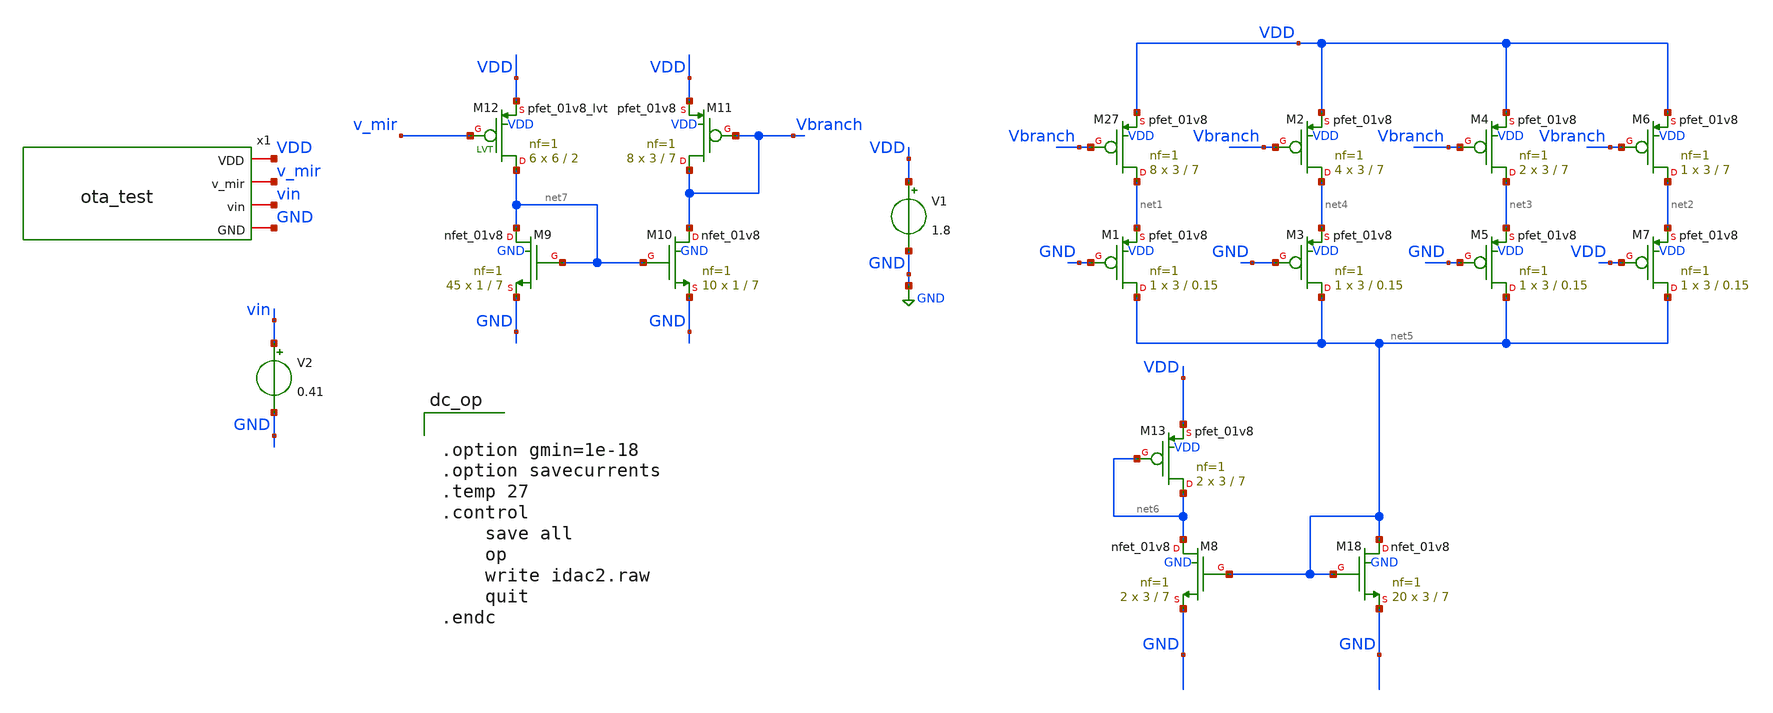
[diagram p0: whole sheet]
** sch_path: xschem/archive/old_blocks/idac2.sch
**.subckt idac2
XM27 net1 Vbranch VDD VDD sky130_fd_pr__pfet_01v8 L=7 W=3 nf=1 ad='int((1 + 1)/2) * 3 / 1 * 0.29' as='int((1 + 2)/2) * 3 / 1 * 0.29'
+ pd='2*int((1 + 1)/2) * (3 / 1 + 0.29)' ps='2*int((1 + 2)/2) * (3 / 1 + 0.29)' nrd='0.29 / 3 ' nrs='0.29 / 3 '
+ sa=0 sb=0 sd=0 mult=8 m=8
XM1 net5 GND net1 VDD sky130_fd_pr__pfet_01v8 L=0.15 W=3 nf=1 ad='int((1 + 1)/2) * 3 / 1 * 0.29' as='int((1 + 2)/2) * 3 / 1 * 0.29'
+ pd='2*int((1 + 1)/2) * (3 / 1 + 0.29)' ps='2*int((1 + 2)/2) * (3 / 1 + 0.29)' nrd='0.29 / 3 ' nrs='0.29 / 3 '
+ sa=0 sb=0 sd=0 mult=1 m=1
XM2 net4 Vbranch VDD VDD sky130_fd_pr__pfet_01v8 L=7 W=3 nf=1 ad='int((1 + 1)/2) * 3 / 1 * 0.29' as='int((1 + 2)/2) * 3 / 1 * 0.29'
+ pd='2*int((1 + 1)/2) * (3 / 1 + 0.29)' ps='2*int((1 + 2)/2) * (3 / 1 + 0.29)' nrd='0.29 / 3 ' nrs='0.29 / 3 '
+ sa=0 sb=0 sd=0 mult=4 m=4
XM3 net5 GND net4 VDD sky130_fd_pr__pfet_01v8 L=0.15 W=3 nf=1 ad='int((1 + 1)/2) * 3 / 1 * 0.29' as='int((1 + 2)/2) * 3 / 1 * 0.29'
+ pd='2*int((1 + 1)/2) * (3 / 1 + 0.29)' ps='2*int((1 + 2)/2) * (3 / 1 + 0.29)' nrd='0.29 / 3 ' nrs='0.29 / 3 '
+ sa=0 sb=0 sd=0 mult=1 m=1
XM4 net3 Vbranch VDD VDD sky130_fd_pr__pfet_01v8 L=7 W=3 nf=1 ad='int((1 + 1)/2) * 3 / 1 * 0.29' as='int((1 + 2)/2) * 3 / 1 * 0.29'
+ pd='2*int((1 + 1)/2) * (3 / 1 + 0.29)' ps='2*int((1 + 2)/2) * (3 / 1 + 0.29)' nrd='0.29 / 3 ' nrs='0.29 / 3 '
+ sa=0 sb=0 sd=0 mult=2 m=2
XM5 net5 GND net3 VDD sky130_fd_pr__pfet_01v8 L=0.15 W=3 nf=1 ad='int((1 + 1)/2) * 3 / 1 * 0.29' as='int((1 + 2)/2) * 3 / 1 * 0.29'
+ pd='2*int((1 + 1)/2) * (3 / 1 + 0.29)' ps='2*int((1 + 2)/2) * (3 / 1 + 0.29)' nrd='0.29 / 3 ' nrs='0.29 / 3 '
+ sa=0 sb=0 sd=0 mult=1 m=1
XM6 net2 Vbranch VDD VDD sky130_fd_pr__pfet_01v8 L=7 W=3 nf=1 ad='int((1 + 1)/2) * 3 / 1 * 0.29' as='int((1 + 2)/2) * 3 / 1 * 0.29'
+ pd='2*int((1 + 1)/2) * (3 / 1 + 0.29)' ps='2*int((1 + 2)/2) * (3 / 1 + 0.29)' nrd='0.29 / 3 ' nrs='0.29 / 3 '
+ sa=0 sb=0 sd=0 mult=1 m=1
XM7 net5 VDD net2 VDD sky130_fd_pr__pfet_01v8 L=0.15 W=3 nf=1 ad='int((1 + 1)/2) * 3 / 1 * 0.29' as='int((1 + 2)/2) * 3 / 1 * 0.29'
+ pd='2*int((1 + 1)/2) * (3 / 1 + 0.29)' ps='2*int((1 + 2)/2) * (3 / 1 + 0.29)' nrd='0.29 / 3 ' nrs='0.29 / 3 '
+ sa=0 sb=0 sd=0 mult=1 m=1
XM18 net5 net5 GND GND sky130_fd_pr__nfet_01v8 L=7 W=3 nf=1 ad='int((nf+1)/2) * W/nf * 0.29' as='int((nf+2)/2) * W/nf * 0.29'
+ pd='2*int((nf+1)/2) * (W/nf + 0.29)' ps='2*int((nf+2)/2) * (W/nf + 0.29)' nrd='0.29 / W' nrs='0.29 / W'
+ sa=0 sb=0 sd=0 mult=20 m=20
XM8 net6 net5 GND GND sky130_fd_pr__nfet_01v8 L=7 W=3 nf=1 ad='int((nf+1)/2) * W/nf * 0.29' as='int((nf+2)/2) * W/nf * 0.29'
+ pd='2*int((nf+1)/2) * (W/nf + 0.29)' ps='2*int((nf+2)/2) * (W/nf + 0.29)' nrd='0.29 / W' nrs='0.29 / W'
+ sa=0 sb=0 sd=0 mult=2 m=2
XM9 net7 net7 GND GND sky130_fd_pr__nfet_01v8 L=7 W=1 nf=1 ad='int((nf+1)/2) * W/nf * 0.29' as='int((nf+2)/2) * W/nf * 0.29'
+ pd='2*int((nf+1)/2) * (W/nf + 0.29)' ps='2*int((nf+2)/2) * (W/nf + 0.29)' nrd='0.29 / W' nrs='0.29 / W'
+ sa=0 sb=0 sd=0 mult=45 m=45
XM10 Vbranch net7 GND GND sky130_fd_pr__nfet_01v8 L=7 W=1 nf=1 ad='int((nf+1)/2) * W/nf * 0.29' as='int((nf+2)/2) * W/nf * 0.29'
+ pd='2*int((nf+1)/2) * (W/nf + 0.29)' ps='2*int((nf+2)/2) * (W/nf + 0.29)' nrd='0.29 / W' nrs='0.29 / W'
+ sa=0 sb=0 sd=0 mult=10 m=10
XM11 Vbranch Vbranch VDD VDD sky130_fd_pr__pfet_01v8 L=7 W=3 nf=1 ad='int((1 + 1)/2) * 3 / 1 * 0.29'
+ as='int((1 + 2)/2) * 3 / 1 * 0.29' pd='2*int((1 + 1)/2) * (3 / 1 + 0.29)' ps='2*int((1 + 2)/2) * (3 / 1 + 0.29)'
+ nrd='0.29 / 3 ' nrs='0.29 / 3 ' sa=0 sb=0 sd=0 mult=8 m=8
V1 VDD GND 1.8
x1 VDD v_mir vin GND ota_test
XM12 net7 v_mir VDD VDD sky130_fd_pr__pfet_01v8_lvt L=2 W=6 nf=1 ad='int((1 + 1)/2) * 6 / 1 * 0.29' as='int((1 + 2)/2) * 6 / 1 * 0.29'
+ pd='2*int((1 + 1)/2) * (6 / 1 + 0.29)' ps='2*int((1 + 2)/2) * (6 / 1 + 0.29)' nrd='0.29 / 6 ' nrs='0.29 / 6 '
+ sa=0 sb=0 sd=0 mult=6 m=6
V2 vin GND 0.41
XM13 net6 net6 VDD VDD sky130_fd_pr__pfet_01v8 L=7 W=3 nf=1 ad='int((1 + 1)/2) * 3 / 1 * 0.29' as='int((1 + 2)/2) * 3 / 1 * 0.29'
+ pd='2*int((1 + 1)/2) * (3 / 1 + 0.29)' ps='2*int((1 + 2)/2) * (3 / 1 + 0.29)' nrd='0.29 / 3 ' nrs='0.29 / 3 '
+ sa=0 sb=0 sd=0 mult=2 m=2
**** begin user architecture code


.option gmin=1e-18
.option savecurrents
.temp 27
.control
    save all
    op
    write idac2.raw
    quit
.endc




** opencircuitdesign pdks install
.lib $::SKYWATER_MODELS/sky130.lib.spice ss

**** end user architecture code
**.ends

* expanding   symbol:  ota_test.sym # of pins=4
** sym_path: xschem/archive/old_blocks/ota_test.sym
** sch_path: xschem/archive/old_blocks/ota_test.sch
.subckt ota_test VDD v_mir vin GND
*.iopin v_mir
*.iopin vin
*.iopin GND
*.iopin VDD
XR1 GND net2 GND sky130_fd_pr__res_xhigh_po_1p41 L=20 mult=1 m=1
Vmeas VDD net3 0
.save i(vmeas)
XM2 v_mir net1 net2 GND sky130_fd_pr__nfet_01v8_lvt L=1 W=3 nf=1 ad='int((1 + 1)/2) * 3 / 1 * 0.29' as='int((1 + 2)/2) * 3 / 1 * 0.29'
+ pd='2*int((1 + 1)/2) * (3 / 1 + 0.29)' ps='2*int((1 + 2)/2) * (3 / 1 + 0.29)' nrd='0.29 / 3 ' nrs='0.29 / 3 '
+ sa=0 sb=0 sd=0 mult=6 m=6
XM1 v_mir v_mir net3 VDD sky130_fd_pr__pfet_01v8_lvt L=2 W=6 nf=1 ad='int((1 + 1)/2) * 6 / 1 * 0.29'
+ as='int((1 + 2)/2) * 6 / 1 * 0.29' pd='2*int((1 + 1)/2) * (6 / 1 + 0.29)' ps='2*int((1 + 2)/2) * (6 / 1 + 0.29)'
+ nrd='0.29 / 6 ' nrs='0.29 / 6 ' sa=0 sb=0 sd=0 mult=6 m=6
x1 VDD VDD net1 vin net2 net4 GND OTA_Gm_Cell_v2
.ends


* expanding   symbol:  archive/ota_gm_cell/OTA_Gm_Cell_v2.sym # of pins=7
** sym_path: xschem/archive/ota_gm_cell/OTA_Gm_Cell_v2.sym
** sch_path: xschem/archive/ota_gm_cell/OTA_Gm_Cell_v2.sch
.subckt OTA_Gm_Cell_v2 AVDDH EN VOUT VINP VINN MN_TAIL_BIAS GNDA
*.iopin AVDDH
*.iopin GNDA
*.iopin VOUT
*.iopin MN_TAIL_BIAS
*.ipin EN
*.iopin VINP
*.iopin VINN
XM1 VBP_TOP MN_TAIL_BIAS net4 GND sky130_fd_pr__nfet_01v8 L=4 W=10 nf=1 ad='int((1 + 1)/2) * 10 / 1 * 0.29'
+ as='int((1 + 2)/2) * 10 / 1 * 0.29' pd='2*int((1 + 1)/2) * (10 / 1 + 0.29)' ps='2*int((1 + 2)/2) * (10 / 1 + 0.29)'
+ nrd='0.29 / 10 ' nrs='0.29 / 10 ' sa=0 sb=0 sd=0 mult=16 m=16
XM3 net1 VBP_TOP AVDDH VDD sky130_fd_pr__pfet_01v8 L=2 W=2 nf=1 ad='int((1 + 1)/2) * 2 / 1 * 0.29' as='int((1 + 2)/2) * 2 / 1 * 0.29'
+ pd='2*int((1 + 1)/2) * (2 / 1 + 0.29)' ps='2*int((1 + 2)/2) * (2 / 1 + 0.29)' nrd='0.29 / 2 ' nrs='0.29 / 2 '
+ sa=0 sb=0 sd=0 mult=4 m=4
XM4 net2 VBP_TOP AVDDH VDD sky130_fd_pr__pfet_01v8 L=2 W=2 nf=1 ad='int((1 + 1)/2) * 2 / 1 * 0.29' as='int((1 + 2)/2) * 2 / 1 * 0.29'
+ pd='2*int((1 + 1)/2) * (2 / 1 + 0.29)' ps='2*int((1 + 2)/2) * (2 / 1 + 0.29)' nrd='0.29 / 2 ' nrs='0.29 / 2 '
+ sa=0 sb=0 sd=0 mult=1 m=1
XM5 VBP_TOP VBP_CASC net1 VDD sky130_fd_pr__pfet_01v8 L=2 W=2 nf=1 ad='int((1 + 1)/2) * 2 / 1 * 0.29'
+ as='int((1 + 2)/2) * 2 / 1 * 0.29' pd='2*int((1 + 1)/2) * (2 / 1 + 0.29)' ps='2*int((1 + 2)/2) * (2 / 1 + 0.29)'
+ nrd='0.29 / 2 ' nrs='0.29 / 2 ' sa=0 sb=0 sd=0 mult=2 m=2
XM6 net11 VBP_CASC net2 VDD sky130_fd_pr__pfet_01v8 L=2 W=2 nf=1 ad='int((1 + 1)/2) * 2 / 1 * 0.29' as='int((1 + 2)/2) * 2 / 1 * 0.29'
+ pd='2*int((1 + 1)/2) * (2 / 1 + 0.29)' ps='2*int((1 + 2)/2) * (2 / 1 + 0.29)' nrd='0.29 / 2 ' nrs='0.29 / 2 '
+ sa=0 sb=0 sd=0 mult=2 m=2
XM7 VOUT MN_TAIL_BIAS net5 GND sky130_fd_pr__nfet_01v8 L=4 W=10 nf=1 ad='int((1 + 1)/2) * 10 / 1 * 0.29'
+ as='int((1 + 2)/2) * 10 / 1 * 0.29' pd='2*int((1 + 1)/2) * (10 / 1 + 0.29)' ps='2*int((1 + 2)/2) * (10 / 1 + 0.29)'
+ nrd='0.29 / 10 ' nrs='0.29 / 10 ' sa=0 sb=0 sd=0 mult=16 m=16
XM10 MN_TAIL_BIAS MN_TAIL_BIAS GNDA GND sky130_fd_pr__nfet_01v8 L=4 W=10 nf=1 ad='int((1 + 1)/2) * 10 / 1 * 0.29'
+ as='int((1 + 2)/2) * 10 / 1 * 0.29' pd='2*int((1 + 1)/2) * (10 / 1 + 0.29)' ps='2*int((1 + 2)/2) * (10 / 1 + 0.29)'
+ nrd='0.29 / 10 ' nrs='0.29 / 10 ' sa=0 sb=0 sd=0 mult=4 m=4
XM12 MN_TAIL_BIAS VSTRP_OUT net10 VDD sky130_fd_pr__pfet_01v8 L=4 W=0.5 nf=1 ad='int((1 + 1)/2) * 0.5 / 1 * 0.29'
+ as='int((1 + 2)/2) * 0.5 / 1 * 0.29' pd='2*int((1 + 1)/2) * (0.5 / 1 + 0.29)' ps='2*int((1 + 2)/2) * (0.5 / 1 + 0.29)'
+ nrd='0.29 / 0.5 ' nrs='0.29 / 0.5 ' sa=0 sb=0 sd=0 mult=1 m=1
XM15 VBP_TOP EN AVDDH VDD sky130_fd_pr__pfet_01v8 L=1 W=0.5 nf=1 ad='int((1 + 1)/2) * 0.5 / 1 * 0.29'
+ as='int((1 + 2)/2) * 0.5 / 1 * 0.29' pd='2*int((1 + 1)/2) * (0.5 / 1 + 0.29)' ps='2*int((1 + 2)/2) * (0.5 / 1 + 0.29)'
+ nrd='0.29 / 0.5 ' nrs='0.29 / 0.5 ' sa=0 sb=0 sd=0 mult=1 m=1
XM16 MN_TAIL_BIAS EN_B GNDA GND sky130_fd_pr__nfet_01v8 L=6.4 W=0.5 nf=1 ad='int((1 + 1)/2) * 0.5 / 1 * 0.29'
+ as='int((1 + 2)/2) * 0.5 / 1 * 0.29' pd='2*int((1 + 1)/2) * (0.5 / 1 + 0.29)' ps='2*int((1 + 2)/2) * (0.5 / 1 + 0.29)'
+ nrd='0.29 / 0.5 ' nrs='0.29 / 0.5 ' sa=0 sb=0 sd=0 mult=1 m=1
XM8 net3 VBP_TOP AVDDH VDD sky130_fd_pr__pfet_01v8 L=2 W=2 nf=1 ad='int((1 + 1)/2) * 2 / 1 * 0.29' as='int((1 + 2)/2) * 2 / 1 * 0.29'
+ pd='2*int((1 + 1)/2) * (2 / 1 + 0.29)' ps='2*int((1 + 2)/2) * (2 / 1 + 0.29)' nrd='0.29 / 2 ' nrs='0.29 / 2 '
+ sa=0 sb=0 sd=0 mult=4 m=4
XM9 VOUT VBP_CASC net3 VDD sky130_fd_pr__pfet_01v8 L=2 W=2 nf=1 ad='int((1 + 1)/2) * 2 / 1 * 0.29' as='int((1 + 2)/2) * 2 / 1 * 0.29'
+ pd='2*int((1 + 1)/2) * (2 / 1 + 0.29)' ps='2*int((1 + 2)/2) * (2 / 1 + 0.29)' nrd='0.29 / 2 ' nrs='0.29 / 2 '
+ sa=0 sb=0 sd=0 mult=2 m=2
XR8 net12 net4 GNDA sky130_fd_pr__res_xhigh_po_1p41 L=6.4 mult=1 m=1
XR10 net13 net12 GNDA sky130_fd_pr__res_xhigh_po_1p41 L=6.4 mult=1 m=1
XR11 net14 net13 GNDA sky130_fd_pr__res_xhigh_po_1p41 L=6.4 mult=1 m=1
XR12 net15 net14 GNDA sky130_fd_pr__res_xhigh_po_1p41 L=6.4 mult=1 m=1
XR13 net16 net15 GNDA sky130_fd_pr__res_xhigh_po_1p41 L=6.4 mult=1 m=1
XR14 net17 net16 GNDA sky130_fd_pr__res_xhigh_po_1p41 L=6.4 mult=1 m=1
XR15 net18 net17 GNDA sky130_fd_pr__res_xhigh_po_1p41 L=6.4 mult=1 m=1
XR16 net19 net18 GNDA sky130_fd_pr__res_xhigh_po_1p41 L=6.4 mult=1 m=1
XR17 GNDA net19 GNDA sky130_fd_pr__res_xhigh_po_1p41 L=6.4 mult=1 m=1
XR1 net20 AVDDH GNDA sky130_fd_pr__res_xhigh_po_1p41 L=7.05 mult=1 m=1
XR3 net21 net20 GNDA sky130_fd_pr__res_xhigh_po_1p41 L=7.05 mult=1 m=1
XR4 net22 net21 GNDA sky130_fd_pr__res_xhigh_po_1p41 L=7.05 mult=1 m=1
XR7 net23 net22 GNDA sky130_fd_pr__res_xhigh_po_1p41 L=7.05 mult=1 m=1
XR18 net24 net23 GNDA sky130_fd_pr__res_xhigh_po_1p41 L=7.05 mult=1 m=1
XR19 net25 net24 GNDA sky130_fd_pr__res_xhigh_po_1p41 L=7.05 mult=1 m=1
XR20 net26 net25 GNDA sky130_fd_pr__res_xhigh_po_1p41 L=7.05 mult=1 m=1
XR21 net27 net26 GNDA sky130_fd_pr__res_xhigh_po_1p41 L=7.05 mult=1 m=1
XR22 net10 net27 GNDA sky130_fd_pr__res_xhigh_po_1p41 L=7.05 mult=1 m=1
XR5 net28 net5 GNDA sky130_fd_pr__res_xhigh_po_1p41 L=6.4 mult=1 m=1
XR23 net29 net28 GNDA sky130_fd_pr__res_xhigh_po_1p41 L=6.4 mult=1 m=1
XR24 net30 net29 GNDA sky130_fd_pr__res_xhigh_po_1p41 L=6.4 mult=1 m=1
XR25 net31 net30 GNDA sky130_fd_pr__res_xhigh_po_1p41 L=6.4 mult=1 m=1
XR26 net32 net31 GNDA sky130_fd_pr__res_xhigh_po_1p41 L=6.4 mult=1 m=1
XR27 net33 net32 GNDA sky130_fd_pr__res_xhigh_po_1p41 L=6.4 mult=1 m=1
XR28 net34 net33 GNDA sky130_fd_pr__res_xhigh_po_1p41 L=6.4 mult=1 m=1
XR29 net35 net34 GNDA sky130_fd_pr__res_xhigh_po_1p41 L=6.4 mult=1 m=1
XR30 GNDA net35 GNDA sky130_fd_pr__res_xhigh_po_1p41 L=6.4 mult=1 m=1
XM2 net6 VBP_TOP AVDDH VDD sky130_fd_pr__pfet_01v8 L=2 W=2 nf=1 ad='int((1 + 1)/2) * 2 / 1 * 0.29' as='int((1 + 2)/2) * 2 / 1 * 0.29'
+ pd='2*int((1 + 1)/2) * (2 / 1 + 0.29)' ps='2*int((1 + 2)/2) * (2 / 1 + 0.29)' nrd='0.29 / 2 ' nrs='0.29 / 2 '
+ sa=0 sb=0 sd=0 mult=7 m=7
XM11 VSTRP_IP VBP_CASC net6 VDD sky130_fd_pr__pfet_01v8 L=2 W=2 nf=1 ad='int((1 + 1)/2) * 2 / 1 * 0.29'
+ as='int((1 + 2)/2) * 2 / 1 * 0.29' pd='2*int((1 + 1)/2) * (2 / 1 + 0.29)' ps='2*int((1 + 2)/2) * (2 / 1 + 0.29)'
+ nrd='0.29 / 2 ' nrs='0.29 / 2 ' sa=0 sb=0 sd=0 mult=14 m=14
XM19 VSTRP_IP AVDDH net36 GNDA sky130_fd_pr__nfet_01v8 L=10 W=0.5 nf=1 ad='int((1 + 1)/2) * 0.5 / 1 * 0.29'
+ as='int((1 + 2)/2) * 0.5 / 1 * 0.29' pd='2*int((1 + 1)/2) * (0.5 / 1 + 0.29)' ps='2*int((1 + 2)/2) * (0.5 / 1 + 0.29)'
+ nrd='0.29 / 0.5 ' nrs='0.29 / 0.5 ' sa=0 sb=0 sd=0 mult=1 m=1
XM20 net36 AVDDH net37 GNDA sky130_fd_pr__nfet_01v8 L=10 W=0.5 nf=1 ad='int((1 + 1)/2) * 0.5 / 1 * 0.29'
+ as='int((1 + 2)/2) * 0.5 / 1 * 0.29' pd='2*int((1 + 1)/2) * (0.5 / 1 + 0.29)' ps='2*int((1 + 2)/2) * (0.5 / 1 + 0.29)'
+ nrd='0.29 / 0.5 ' nrs='0.29 / 0.5 ' sa=0 sb=0 sd=0 mult=1 m=1
XM21 net37 AVDDH net38 GNDA sky130_fd_pr__nfet_01v8 L=10 W=0.5 nf=1 ad='int((1 + 1)/2) * 0.5 / 1 * 0.29'
+ as='int((1 + 2)/2) * 0.5 / 1 * 0.29' pd='2*int((1 + 1)/2) * (0.5 / 1 + 0.29)' ps='2*int((1 + 2)/2) * (0.5 / 1 + 0.29)'
+ nrd='0.29 / 0.5 ' nrs='0.29 / 0.5 ' sa=0 sb=0 sd=0 mult=1 m=1
XM26 net38 AVDDH net39 GNDA sky130_fd_pr__nfet_01v8 L=10 W=0.5 nf=1 ad='int((1 + 1)/2) * 0.5 / 1 * 0.29'
+ as='int((1 + 2)/2) * 0.5 / 1 * 0.29' pd='2*int((1 + 1)/2) * (0.5 / 1 + 0.29)' ps='2*int((1 + 2)/2) * (0.5 / 1 + 0.29)'
+ nrd='0.29 / 0.5 ' nrs='0.29 / 0.5 ' sa=0 sb=0 sd=0 mult=1 m=1
XM27 net39 AVDDH net40 GNDA sky130_fd_pr__nfet_01v8 L=10 W=0.5 nf=1 ad='int((1 + 1)/2) * 0.5 / 1 * 0.29'
+ as='int((1 + 2)/2) * 0.5 / 1 * 0.29' pd='2*int((1 + 1)/2) * (0.5 / 1 + 0.29)' ps='2*int((1 + 2)/2) * (0.5 / 1 + 0.29)'
+ nrd='0.29 / 0.5 ' nrs='0.29 / 0.5 ' sa=0 sb=0 sd=0 mult=1 m=1
XM28 net40 AVDDH net41 GNDA sky130_fd_pr__nfet_01v8 L=10 W=0.5 nf=1 ad='int((1 + 1)/2) * 0.5 / 1 * 0.29'
+ as='int((1 + 2)/2) * 0.5 / 1 * 0.29' pd='2*int((1 + 1)/2) * (0.5 / 1 + 0.29)' ps='2*int((1 + 2)/2) * (0.5 / 1 + 0.29)'
+ nrd='0.29 / 0.5 ' nrs='0.29 / 0.5 ' sa=0 sb=0 sd=0 mult=1 m=1
XM29 net41 AVDDH net42 GNDA sky130_fd_pr__nfet_01v8 L=10 W=0.5 nf=1 ad='int((1 + 1)/2) * 0.5 / 1 * 0.29'
+ as='int((1 + 2)/2) * 0.5 / 1 * 0.29' pd='2*int((1 + 1)/2) * (0.5 / 1 + 0.29)' ps='2*int((1 + 2)/2) * (0.5 / 1 + 0.29)'
+ nrd='0.29 / 0.5 ' nrs='0.29 / 0.5 ' sa=0 sb=0 sd=0 mult=1 m=1
XM30 net42 AVDDH net43 GNDA sky130_fd_pr__nfet_01v8 L=10 W=0.5 nf=1 ad='int((1 + 1)/2) * 0.5 / 1 * 0.29'
+ as='int((1 + 2)/2) * 0.5 / 1 * 0.29' pd='2*int((1 + 1)/2) * (0.5 / 1 + 0.29)' ps='2*int((1 + 2)/2) * (0.5 / 1 + 0.29)'
+ nrd='0.29 / 0.5 ' nrs='0.29 / 0.5 ' sa=0 sb=0 sd=0 mult=1 m=1
XM31 net43 AVDDH net44 GNDA sky130_fd_pr__nfet_01v8 L=10 W=0.5 nf=1 ad='int((1 + 1)/2) * 0.5 / 1 * 0.29'
+ as='int((1 + 2)/2) * 0.5 / 1 * 0.29' pd='2*int((1 + 1)/2) * (0.5 / 1 + 0.29)' ps='2*int((1 + 2)/2) * (0.5 / 1 + 0.29)'
+ nrd='0.29 / 0.5 ' nrs='0.29 / 0.5 ' sa=0 sb=0 sd=0 mult=1 m=1
XM32 net44 AVDDH GNDA GNDA sky130_fd_pr__nfet_01v8 L=10 W=0.5 nf=1 ad='int((1 + 1)/2) * 0.5 / 1 * 0.29'
+ as='int((1 + 2)/2) * 0.5 / 1 * 0.29' pd='2*int((1 + 1)/2) * (0.5 / 1 + 0.29)' ps='2*int((1 + 2)/2) * (0.5 / 1 + 0.29)'
+ nrd='0.29 / 0.5 ' nrs='0.29 / 0.5 ' sa=0 sb=0 sd=0 mult=1 m=1
XM33 net1 VINP net7 GND sky130_fd_pr__nfet_01v8_lvt L=2 W=2 nf=1 ad='int((1 + 1)/2) * 2 / 1 * 0.29' as='int((1 + 2)/2) * 2 / 1 * 0.29'
+ pd='2*int((1 + 1)/2) * (2 / 1 + 0.29)' ps='2*int((1 + 2)/2) * (2 / 1 + 0.29)' nrd='0.29 / 2 ' nrs='0.29 / 2 '
+ sa=0 sb=0 sd=0 mult=8 m=8
XM34 net3 VINN net7 GND sky130_fd_pr__nfet_01v8_lvt L=2 W=2 nf=1 ad='int((1 + 1)/2) * 2 / 1 * 0.29' as='int((1 + 2)/2) * 2 / 1 * 0.29'
+ pd='2*int((1 + 1)/2) * (2 / 1 + 0.29)' ps='2*int((1 + 2)/2) * (2 / 1 + 0.29)' nrd='0.29 / 2 ' nrs='0.29 / 2 '
+ sa=0 sb=0 sd=0 mult=8 m=8
XM35 net7 MN_TAIL_BIAS GNDA GND sky130_fd_pr__nfet_01v8 L=4 W=10 nf=1 ad='int((1 + 1)/2) * 10 / 1 * 0.29'
+ as='int((1 + 2)/2) * 10 / 1 * 0.29' pd='2*int((1 + 1)/2) * (10 / 1 + 0.29)' ps='2*int((1 + 2)/2) * (10 / 1 + 0.29)'
+ nrd='0.29 / 10 ' nrs='0.29 / 10 ' sa=0 sb=0 sd=0 mult=24 m=24
XM36 EN_B EN GNDA GND sky130_fd_pr__nfet_01v8 L=0.15 W=1 nf=1 ad='int((1 + 1)/2) * 1 / 1 * 0.29' as='int((1 + 2)/2) * 1 / 1 * 0.29'
+ pd='2*int((1 + 1)/2) * (1 / 1 + 0.29)' ps='2*int((1 + 2)/2) * (1 / 1 + 0.29)' nrd='0.29 / 1 ' nrs='0.29 / 1 '
+ sa=0 sb=0 sd=0 mult=1 m=1
XM37 EN_B EN AVDDH VDD sky130_fd_pr__pfet_01v8 L=0.15 W=1 nf=1 ad='int((1 + 1)/2) * 1 / 1 * 0.29' as='int((1 + 2)/2) * 1 / 1 * 0.29'
+ pd='2*int((1 + 1)/2) * (1 / 1 + 0.29)' ps='2*int((1 + 2)/2) * (1 / 1 + 0.29)' nrd='0.29 / 1 ' nrs='0.29 / 1 '
+ sa=0 sb=0 sd=0 mult=1 m=1
XM38 VSTRP_OUT net9 net8 GND sky130_fd_pr__nfet_01v8 L=0.15 W=1 nf=1 ad='int((1 + 1)/2) * 1 / 1 * 0.29'
+ as='int((1 + 2)/2) * 1 / 1 * 0.29' pd='2*int((1 + 1)/2) * (1 / 1 + 0.29)' ps='2*int((1 + 2)/2) * (1 / 1 + 0.29)'
+ nrd='0.29 / 1 ' nrs='0.29 / 1 ' sa=0 sb=0 sd=0 mult=1 m=1
XM39 net8 EN GNDA GND sky130_fd_pr__nfet_01v8 L=0.15 W=1 nf=1 ad='int((1 + 1)/2) * 1 / 1 * 0.29' as='int((1 + 2)/2) * 1 / 1 * 0.29'
+ pd='2*int((1 + 1)/2) * (1 / 1 + 0.29)' ps='2*int((1 + 2)/2) * (1 / 1 + 0.29)' nrd='0.29 / 1 ' nrs='0.29 / 1 '
+ sa=0 sb=0 sd=0 mult=1 m=1
XM42 net9 VSTRP_IP GNDA GND sky130_fd_pr__nfet_01v8 L=0.15 W=1 nf=1 ad='int((1 + 1)/2) * 1 / 1 * 0.29'
+ as='int((1 + 2)/2) * 1 / 1 * 0.29' pd='2*int((1 + 1)/2) * (1 / 1 + 0.29)' ps='2*int((1 + 2)/2) * (1 / 1 + 0.29)'
+ nrd='0.29 / 1 ' nrs='0.29 / 1 ' sa=0 sb=0 sd=0 mult=1 m=1
XM43 net9 VSTRP_IP AVDDH VDD sky130_fd_pr__pfet_01v8 L=0.15 W=1 nf=1 ad='int((1 + 1)/2) * 1 / 1 * 0.29'
+ as='int((1 + 2)/2) * 1 / 1 * 0.29' pd='2*int((1 + 1)/2) * (1 / 1 + 0.29)' ps='2*int((1 + 2)/2) * (1 / 1 + 0.29)'
+ nrd='0.29 / 1 ' nrs='0.29 / 1 ' sa=0 sb=0 sd=0 mult=1 m=1
XM44 net45 VBP_CASC net46 VDD sky130_fd_pr__pfet_01v8 L=2 W=2 nf=1 ad='int((1 + 1)/2) * 2 / 1 * 0.29'
+ as='int((1 + 2)/2) * 2 / 1 * 0.29' pd='2*int((1 + 1)/2) * (2 / 1 + 0.29)' ps='2*int((1 + 2)/2) * (2 / 1 + 0.29)'
+ nrd='0.29 / 2 ' nrs='0.29 / 2 ' sa=0 sb=0 sd=0 mult=1 m=1
XM45 VBP_CASC MN_TAIL_BIAS GNDA GND sky130_fd_pr__nfet_01v8 L=4 W=10 nf=1 ad='int((1 + 1)/2) * 10 / 1 * 0.29'
+ as='int((1 + 2)/2) * 10 / 1 * 0.29' pd='2*int((1 + 1)/2) * (10 / 1 + 0.29)' ps='2*int((1 + 2)/2) * (10 / 1 + 0.29)'
+ nrd='0.29 / 10 ' nrs='0.29 / 10 ' sa=0 sb=0 sd=0 mult=4 m=4
XM46 net47 VBP_CASC net45 VDD sky130_fd_pr__pfet_01v8 L=2 W=2 nf=1 ad='int((1 + 1)/2) * 2 / 1 * 0.29'
+ as='int((1 + 2)/2) * 2 / 1 * 0.29' pd='2*int((1 + 1)/2) * (2 / 1 + 0.29)' ps='2*int((1 + 2)/2) * (2 / 1 + 0.29)'
+ nrd='0.29 / 2 ' nrs='0.29 / 2 ' sa=0 sb=0 sd=0 mult=1 m=1
XM47 VBP_CASC VBP_CASC net47 VDD sky130_fd_pr__pfet_01v8 L=2 W=2 nf=1 ad='int((1 + 1)/2) * 2 / 1 * 0.29'
+ as='int((1 + 2)/2) * 2 / 1 * 0.29' pd='2*int((1 + 1)/2) * (2 / 1 + 0.29)' ps='2*int((1 + 2)/2) * (2 / 1 + 0.29)'
+ nrd='0.29 / 2 ' nrs='0.29 / 2 ' sa=0 sb=0 sd=0 mult=1 m=1
XM48 net48 VBP_CASC net49 VDD sky130_fd_pr__pfet_01v8 L=2 W=2 nf=1 ad='int((1 + 1)/2) * 2 / 1 * 0.29'
+ as='int((1 + 2)/2) * 2 / 1 * 0.29' pd='2*int((1 + 1)/2) * (2 / 1 + 0.29)' ps='2*int((1 + 2)/2) * (2 / 1 + 0.29)'
+ nrd='0.29 / 2 ' nrs='0.29 / 2 ' sa=0 sb=0 sd=0 mult=1 m=1
XM49 net46 VBP_CASC net50 VDD sky130_fd_pr__pfet_01v8 L=2 W=2 nf=1 ad='int((1 + 1)/2) * 2 / 1 * 0.29'
+ as='int((1 + 2)/2) * 2 / 1 * 0.29' pd='2*int((1 + 1)/2) * (2 / 1 + 0.29)' ps='2*int((1 + 2)/2) * (2 / 1 + 0.29)'
+ nrd='0.29 / 2 ' nrs='0.29 / 2 ' sa=0 sb=0 sd=0 mult=1 m=1
XM50 net50 VBP_CASC net48 VDD sky130_fd_pr__pfet_01v8 L=2 W=2 nf=1 ad='int((1 + 1)/2) * 2 / 1 * 0.29'
+ as='int((1 + 2)/2) * 2 / 1 * 0.29' pd='2*int((1 + 1)/2) * (2 / 1 + 0.29)' ps='2*int((1 + 2)/2) * (2 / 1 + 0.29)'
+ nrd='0.29 / 2 ' nrs='0.29 / 2 ' sa=0 sb=0 sd=0 mult=1 m=1
XM51 net49 VBP_CASC AVDDH VDD sky130_fd_pr__pfet_01v8 L=2 W=2 nf=1 ad='int((1 + 1)/2) * 2 / 1 * 0.29'
+ as='int((1 + 2)/2) * 2 / 1 * 0.29' pd='2*int((1 + 1)/2) * (2 / 1 + 0.29)' ps='2*int((1 + 2)/2) * (2 / 1 + 0.29)'
+ nrd='0.29 / 2 ' nrs='0.29 / 2 ' sa=0 sb=0 sd=0 mult=1 m=1
XM13 VSTRP_OUT net9 AVDDH VDD sky130_fd_pr__pfet_01v8 L=0.15 W=1 nf=1 ad='int((1 + 1)/2) * 1 / 1 * 0.29'
+ as='int((1 + 2)/2) * 1 / 1 * 0.29' pd='2*int((1 + 1)/2) * (1 / 1 + 0.29)' ps='2*int((1 + 2)/2) * (1 / 1 + 0.29)'
+ nrd='0.29 / 1 ' nrs='0.29 / 1 ' sa=0 sb=0 sd=0 mult=1 m=1
XM14 VSTRP_OUT EN_B AVDDH VDD sky130_fd_pr__pfet_01v8 L=0.15 W=1 nf=1 ad='int((1 + 1)/2) * 1 / 1 * 0.29'
+ as='int((1 + 2)/2) * 1 / 1 * 0.29' pd='2*int((1 + 1)/2) * (1 / 1 + 0.29)' ps='2*int((1 + 2)/2) * (1 / 1 + 0.29)'
+ nrd='0.29 / 1 ' nrs='0.29 / 1 ' sa=0 sb=0 sd=0 mult=1 m=1
Vmeas net11 MN_TAIL_BIAS 0
.save i(vmeas)
.ends

.GLOBAL GND
.end
